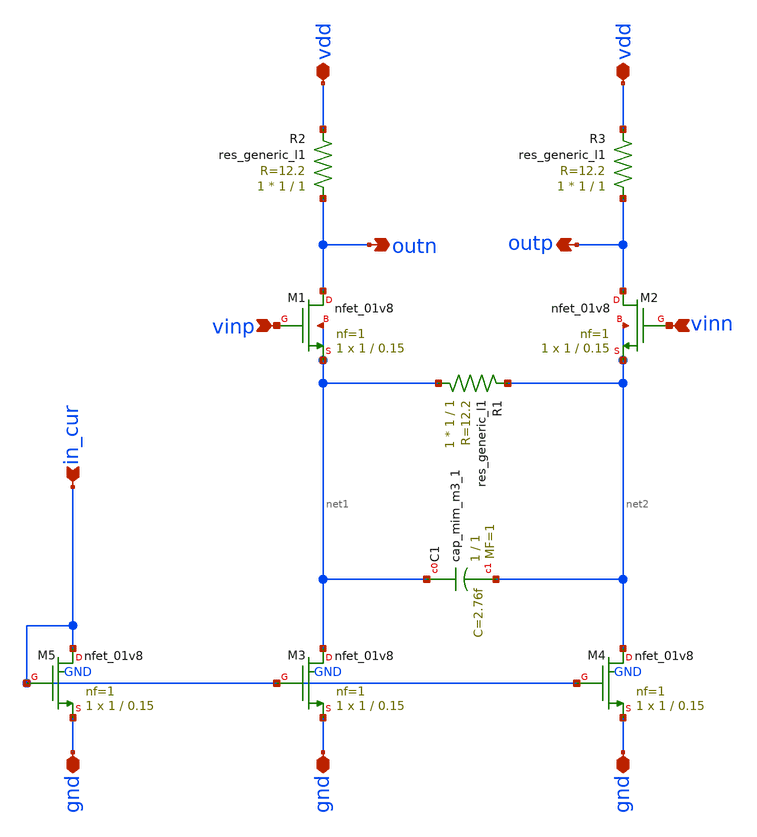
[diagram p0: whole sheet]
** sch_path: CTLE/ctle-base.sch
**.subckt ctle-base vdd vdd gnd gnd gnd vinp vinn outn outp in_cur
*.iopin vdd
*.iopin vdd
*.iopin gnd
*.iopin gnd
*.iopin gnd
*.ipin vinp
*.ipin vinn
*.opin outn
*.opin outp
*.ipin in_cur
XM1 outn vinp net1 net1 sky130_fd_pr__nfet_01v8 L=0.15 W=1 nf=1 ad='int((nf+1)/2) * W/nf * 0.29' as='int((nf+2)/2) * W/nf * 0.29'
+ pd='2*int((nf+1)/2) * (W/nf + 0.29)' ps='2*int((nf+2)/2) * (W/nf + 0.29)' nrd='0.29 / W' nrs='0.29 / W'
+ sa=0 sb=0 sd=0 mult=1 m=1
XM2 outp vinn net2 net2 sky130_fd_pr__nfet_01v8 L=0.15 W=1 nf=1 ad='int((nf+1)/2) * W/nf * 0.29' as='int((nf+2)/2) * W/nf * 0.29'
+ pd='2*int((nf+1)/2) * (W/nf + 0.29)' ps='2*int((nf+2)/2) * (W/nf + 0.29)' nrd='0.29 / W' nrs='0.29 / W'
+ sa=0 sb=0 sd=0 mult=1 m=1
R1 net1 net2 sky130_fd_pr__res_generic_l1 W=1 L=1 m=1
XC1 net1 net2 sky130_fd_pr__cap_mim_m3_1 W=1 L=1 MF=1 m=1
XM3 net1 in_cur gnd GND sky130_fd_pr__nfet_01v8 L=0.15 W=1 nf=1 ad='int((nf+1)/2) * W/nf * 0.29' as='int((nf+2)/2) * W/nf * 0.29'
+ pd='2*int((nf+1)/2) * (W/nf + 0.29)' ps='2*int((nf+2)/2) * (W/nf + 0.29)' nrd='0.29 / W' nrs='0.29 / W'
+ sa=0 sb=0 sd=0 mult=1 m=1
XM4 net2 in_cur gnd GND sky130_fd_pr__nfet_01v8 L=0.15 W=1 nf=1 ad='int((nf+1)/2) * W/nf * 0.29' as='int((nf+2)/2) * W/nf * 0.29'
+ pd='2*int((nf+1)/2) * (W/nf + 0.29)' ps='2*int((nf+2)/2) * (W/nf + 0.29)' nrd='0.29 / W' nrs='0.29 / W'
+ sa=0 sb=0 sd=0 mult=1 m=1
R2 outn vdd sky130_fd_pr__res_generic_l1 W=1 L=1 m=1
R3 outp vdd sky130_fd_pr__res_generic_l1 W=1 L=1 m=1
XM5 in_cur in_cur gnd GND sky130_fd_pr__nfet_01v8 L=0.15 W=1 nf=1 ad='int((nf+1)/2) * W/nf * 0.29' as='int((nf+2)/2) * W/nf * 0.29'
+ pd='2*int((nf+1)/2) * (W/nf + 0.29)' ps='2*int((nf+2)/2) * (W/nf + 0.29)' nrd='0.29 / W' nrs='0.29 / W'
+ sa=0 sb=0 sd=0 mult=1 m=1
**.ends
.end
